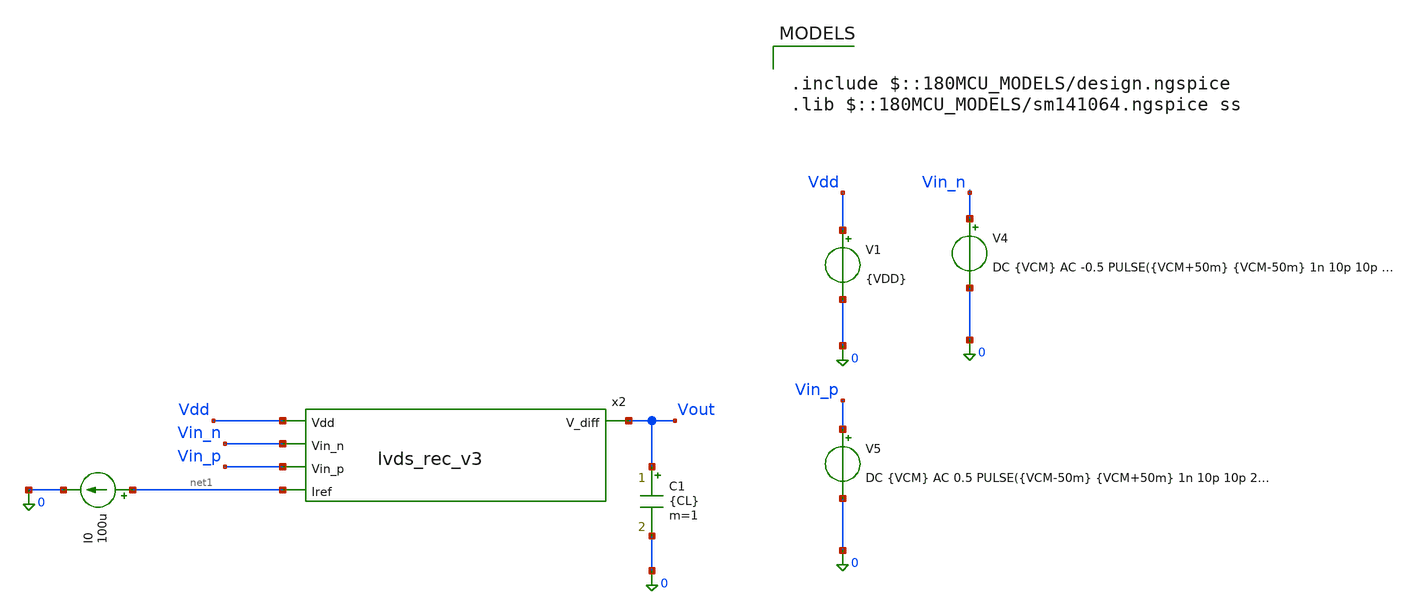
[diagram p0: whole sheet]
** sch_path: blocks/adc/lvds/ota_performance_test.sch
**.subckt ota_performance_test
V1 Vdd 0 {VDD}
V4 Vin_n 0 DC {VCM} AC -0.5 PULSE({VCM+50m} {VCM-50m} 1n 10p 10p 20n 50n)
V5 Vin_p 0 DC {VCM} AC 0.5 PULSE({VCM-50m} {VCM+50m} 1n 10p 10p 20n 50n)
C1 Vout 0 {CL} m=1
I0 net1 0 100u
x2 Vdd Vin_n Vout Vin_p net1 lvds_rec_v3
**** begin user architecture code


.param VDD=3.3
.param VSS=0
.param VCM=1.2
.param VB1=0.0
.param VB2=1.65
.param CL=100f
.options temp=125

.control
save all
set filetype=ascii
set wr_singlescale
shell rm /foss/designs/trans_testing/ota_testing/ota_ac.txt
shell rm /foss/designs/trans_testing/ota_testing/ota_tran.txt

op


* AC gain
ac dec 1000 1 500G
let vin_diff_ac = v(Vin_p)-v(Vin_n)
let gain = v(Vout)/vin_diff_ac
wrdata /foss/designs/trans_testing/ota_testing/ota_ac.txt frequency db(gain) real(gain) imag(gain)
plot v(Vout)

* Transient slew rate
tran 1p 100n
let vin_diff = v(Vin_p)-v(Vin_n)
let slew = deriv(v(Vout))
plot v(Vout)

wrdata /foss/designs/trans_testing/ota_testing/ota_tran.txt time v(Vin_p) v(Vin_n) vin_diff v(Vout)
+ slew

.endc



.include $::180MCU_MODELS/design.ngspice
.lib $::180MCU_MODELS/sm141064.ngspice ss

**** end user architecture code
**.ends

* expanding   symbol:  lvds_rec_v3.sym # of pins=5
** sym_path: blocks/adc/lvds/lvds_rec_v3.sym
** sch_path: blocks/adc/lvds/lvds_rec_v3.sch
.subckt lvds_rec_v3 Vdd Vin_n V_diff Vin_p Iref
*.ipin Vin_p
*.ipin Vin_n
*.opin V_diff
*.ipin Iref
*.ipin Vdd
x1 Vdd net1 Vin_n Vin_p Iref op_amp
x2 Vdd V_diff net1 buffer
.ends


* expanding   symbol:  op_amp.sym # of pins=5
** sym_path: blocks/adc/lvds/op_amp.sym
** sch_path: blocks/adc/lvds/op_amp.sch
.subckt op_amp Vdd Vout Vin_n Vin_p Iref
*.ipin Vdd
*.ipin Vin_p
*.ipin Vin_n
*.opin Vout
*.ipin Iref
XM1 net2 net3 Vdd Vdd pfet_03v3 L=0.28u W=10.5u nf=1 ad='int((nf+1)/2) * W/nf * 0.18u' as='int((nf+2)/2) * W/nf * 0.18u'
+ pd='2*int((nf+1)/2) * (W/nf + 0.18u)' ps='2*int((nf+2)/2) * (W/nf + 0.18u)' nrd='0.18u / W' nrs='0.18u / W'
+ sa=0 sb=0 sd=0 m=1
XM2 net1 net4 Vdd Vdd pfet_03v3 L=0.28u W=10.5u nf=1 ad='int((nf+1)/2) * W/nf * 0.18u' as='int((nf+2)/2) * W/nf * 0.18u'
+ pd='2*int((nf+1)/2) * (W/nf + 0.18u)' ps='2*int((nf+2)/2) * (W/nf + 0.18u)' nrd='0.18u / W' nrs='0.18u / W'
+ sa=0 sb=0 sd=0 m=1
XM3 net3 Vb2 net2 Vdd pfet_03v3 L=0.28u W=10.5u nf=1 ad='int((nf+1)/2) * W/nf * 0.18u' as='int((nf+2)/2) * W/nf * 0.18u'
+ pd='2*int((nf+1)/2) * (W/nf + 0.18u)' ps='2*int((nf+2)/2) * (W/nf + 0.18u)' nrd='0.18u / W' nrs='0.18u / W'
+ sa=0 sb=0 sd=0 m=1
XM4 net4 Vb2 net1 Vdd pfet_03v3 L=0.28u W=10.5u nf=1 ad='int((nf+1)/2) * W/nf * 0.18u' as='int((nf+2)/2) * W/nf * 0.18u'
+ pd='2*int((nf+1)/2) * (W/nf + 0.18u)' ps='2*int((nf+2)/2) * (W/nf + 0.18u)' nrd='0.18u / W' nrs='0.18u / W'
+ sa=0 sb=0 sd=0 m=1
XM5 net4 Vin_p net5 0 nfet_03v3 L=0.28u W=52.5u nf=15 ad='int((nf+1)/2) * W/nf * 0.18u' as='int((nf+2)/2) * W/nf * 0.18u'
+ pd='2*int((nf+1)/2) * (W/nf + 0.18u)' ps='2*int((nf+2)/2) * (W/nf + 0.18u)' nrd='0.18u / W' nrs='0.18u / W'
+ sa=0 sb=0 sd=0 m=1
XM6 net3 Vin_n net5 0 nfet_03v3 L=0.28u W=52.5u nf=15 ad='int((nf+1)/2) * W/nf * 0.18u' as='int((nf+2)/2) * W/nf * 0.18u'
+ pd='2*int((nf+1)/2) * (W/nf + 0.18u)' ps='2*int((nf+2)/2) * (W/nf + 0.18u)' nrd='0.18u / W' nrs='0.18u / W'
+ sa=0 sb=0 sd=0 m=1
XM7 net6 net4 Vdd Vdd pfet_03v3 L=0.28u W=10.5u nf=1 ad='int((nf+1)/2) * W/nf * 0.18u' as='int((nf+2)/2) * W/nf * 0.18u'
+ pd='2*int((nf+1)/2) * (W/nf + 0.18u)' ps='2*int((nf+2)/2) * (W/nf + 0.18u)' nrd='0.18u / W' nrs='0.18u / W'
+ sa=0 sb=0 sd=0 m=1
XM9 net7 net3 Vdd Vdd pfet_03v3 L=0.28u W=10.5u nf=1 ad='int((nf+1)/2) * W/nf * 0.18u' as='int((nf+2)/2) * W/nf * 0.18u'
+ pd='2*int((nf+1)/2) * (W/nf + 0.18u)' ps='2*int((nf+2)/2) * (W/nf + 0.18u)' nrd='0.18u / W' nrs='0.18u / W'
+ sa=0 sb=0 sd=0 m=1
XM11 net8 Vb2 net10 0 nfet_03v3 L=0.28u W=5.25u nf=1 ad='int((nf+1)/2) * W/nf * 0.18u' as='int((nf+2)/2) * W/nf * 0.18u'
+ pd='2*int((nf+1)/2) * (W/nf + 0.18u)' ps='2*int((nf+2)/2) * (W/nf + 0.18u)' nrd='0.18u / W' nrs='0.18u / W'
+ sa=0 sb=0 sd=0 m=1
XM12 Vout Vb2 net9 0 nfet_03v3 L=0.28u W=5.25u nf=1 ad='int((nf+1)/2) * W/nf * 0.18u' as='int((nf+2)/2) * W/nf * 0.18u'
+ pd='2*int((nf+1)/2) * (W/nf + 0.18u)' ps='2*int((nf+2)/2) * (W/nf + 0.18u)' nrd='0.18u / W' nrs='0.18u / W'
+ sa=0 sb=0 sd=0 m=1
XM13 net10 net8 0 0 nfet_03v3 L=0.28u W=5.25u nf=1 ad='int((nf+1)/2) * W/nf * 0.18u' as='int((nf+2)/2) * W/nf * 0.18u'
+ pd='2*int((nf+1)/2) * (W/nf + 0.18u)' ps='2*int((nf+2)/2) * (W/nf + 0.18u)' nrd='0.18u / W' nrs='0.18u / W'
+ sa=0 sb=0 sd=0 m=1
XM14 net9 net8 0 0 nfet_03v3 L=0.28u W=5.25u nf=1 ad='int((nf+1)/2) * W/nf * 0.18u' as='int((nf+2)/2) * W/nf * 0.18u'
+ pd='2*int((nf+1)/2) * (W/nf + 0.18u)' ps='2*int((nf+2)/2) * (W/nf + 0.18u)' nrd='0.18u / W' nrs='0.18u / W'
+ sa=0 sb=0 sd=0 m=1
XM8 net8 0 net6 Vdd pfet_03v3 L=0.28u W=10.5u nf=1 ad='int((nf+1)/2) * W/nf * 0.18u' as='int((nf+2)/2) * W/nf * 0.18u'
+ pd='2*int((nf+1)/2) * (W/nf + 0.18u)' ps='2*int((nf+2)/2) * (W/nf + 0.18u)' nrd='0.18u / W' nrs='0.18u / W'
+ sa=0 sb=0 sd=0 m=1
XM10 Vout 0 net7 Vdd pfet_03v3 L=0.28u W=10.5u nf=1 ad='int((nf+1)/2) * W/nf * 0.18u' as='int((nf+2)/2) * W/nf * 0.18u'
+ pd='2*int((nf+1)/2) * (W/nf + 0.18u)' ps='2*int((nf+2)/2) * (W/nf + 0.18u)' nrd='0.18u / W' nrs='0.18u / W'
+ sa=0 sb=0 sd=0 m=1
XM15 net5 net11 0 0 nfet_03v3 L=1u W=80u nf=20 ad='int((nf+1)/2) * W/nf * 0.18u' as='int((nf+2)/2) * W/nf * 0.18u'
+ pd='2*int((nf+1)/2) * (W/nf + 0.18u)' ps='2*int((nf+2)/2) * (W/nf + 0.18u)' nrd='0.18u / W' nrs='0.18u / W'
+ sa=0 sb=0 sd=0 m=1
XM16 Iref Iref Vdd Vdd pfet_03v3 L=1u W=20u nf=1 ad='int((nf+1)/2) * W/nf * 0.18u' as='int((nf+2)/2) * W/nf * 0.18u'
+ pd='2*int((nf+1)/2) * (W/nf + 0.18u)' ps='2*int((nf+2)/2) * (W/nf + 0.18u)' nrd='0.18u / W' nrs='0.18u / W'
+ sa=0 sb=0 sd=0 m=1
XM17 net11 Iref Vdd Vdd pfet_03v3 L=1u W=80u nf=1 ad='int((nf+1)/2) * W/nf * 0.18u' as='int((nf+2)/2) * W/nf * 0.18u'
+ pd='2*int((nf+1)/2) * (W/nf + 0.18u)' ps='2*int((nf+2)/2) * (W/nf + 0.18u)' nrd='0.18u / W' nrs='0.18u / W'
+ sa=0 sb=0 sd=0 m=1
XM18 Vb2 Iref Vdd Vdd pfet_03v3 L=1u W=20u nf=1 ad='int((nf+1)/2) * W/nf * 0.18u' as='int((nf+2)/2) * W/nf * 0.18u'
+ pd='2*int((nf+1)/2) * (W/nf + 0.18u)' ps='2*int((nf+2)/2) * (W/nf + 0.18u)' nrd='0.18u / W' nrs='0.18u / W'
+ sa=0 sb=0 sd=0 m=1
XM19 Vb2 Vb2 net12 0 nfet_03v3 L=0.28u W=30u nf=1 ad='int((nf+1)/2) * W/nf * 0.18u' as='int((nf+2)/2) * W/nf * 0.18u'
+ pd='2*int((nf+1)/2) * (W/nf + 0.18u)' ps='2*int((nf+2)/2) * (W/nf + 0.18u)' nrd='0.18u / W' nrs='0.18u / W'
+ sa=0 sb=0 sd=0 m=1
XM20 net12 net12 0 0 nfet_03v3 L=0.28u W=30u nf=1 ad='int((nf+1)/2) * W/nf * 0.18u' as='int((nf+2)/2) * W/nf * 0.18u'
+ pd='2*int((nf+1)/2) * (W/nf + 0.18u)' ps='2*int((nf+2)/2) * (W/nf + 0.18u)' nrd='0.18u / W' nrs='0.18u / W'
+ sa=0 sb=0 sd=0 m=1
XM21 net11 net11 0 0 nfet_03v3 L=1u W=80u nf=1 ad='int((nf+1)/2) * W/nf * 0.18u' as='int((nf+2)/2) * W/nf * 0.18u'
+ pd='2*int((nf+1)/2) * (W/nf + 0.18u)' ps='2*int((nf+2)/2) * (W/nf + 0.18u)' nrd='0.18u / W' nrs='0.18u / W'
+ sa=0 sb=0 sd=0 m=1
.ends


* expanding   symbol:  buffer.sym # of pins=3
** sym_path: blocks/adc/lvds/buffer.sym
** sch_path: blocks/adc/lvds/buffer.sch
.subckt buffer Vdd Vout_buff Vin
*.ipin Vdd
*.ipin Vin
*.opin Vout_buff
XM1 net1 Vin Vdd Vdd pfet_03v3 L=0.28u W=0.66u nf=1 ad='int((nf+1)/2) * W/nf * 0.18u' as='int((nf+2)/2) * W/nf * 0.18u'
+ pd='2*int((nf+1)/2) * (W/nf + 0.18u)' ps='2*int((nf+2)/2) * (W/nf + 0.18u)' nrd='0.18u / W' nrs='0.18u / W'
+ sa=0 sb=0 sd=0 m=1
XM2 net1 Vin 0 0 nfet_03v3 L=0.28u W=0.22u nf=1 ad='int((nf+1)/2) * W/nf * 0.18u' as='int((nf+2)/2) * W/nf * 0.18u'
+ pd='2*int((nf+1)/2) * (W/nf + 0.18u)' ps='2*int((nf+2)/2) * (W/nf + 0.18u)' nrd='0.18u / W' nrs='0.18u / W'
+ sa=0 sb=0 sd=0 m=1
XM3 net2 net1 Vdd Vdd pfet_03v3 L=0.28u W=2.64u nf=1 ad='int((nf+1)/2) * W/nf * 0.18u' as='int((nf+2)/2) * W/nf * 0.18u'
+ pd='2*int((nf+1)/2) * (W/nf + 0.18u)' ps='2*int((nf+2)/2) * (W/nf + 0.18u)' nrd='0.18u / W' nrs='0.18u / W'
+ sa=0 sb=0 sd=0 m=1
XM4 net2 net1 0 0 nfet_03v3 L=0.28u W=0.88u nf=1 ad='int((nf+1)/2) * W/nf * 0.18u' as='int((nf+2)/2) * W/nf * 0.18u'
+ pd='2*int((nf+1)/2) * (W/nf + 0.18u)' ps='2*int((nf+2)/2) * (W/nf + 0.18u)' nrd='0.18u / W' nrs='0.18u / W'
+ sa=0 sb=0 sd=0 m=1
XM5 net3 net2 Vdd Vdd pfet_03v3 L=0.28u W=10.56u nf=1 ad='int((nf+1)/2) * W/nf * 0.18u' as='int((nf+2)/2) * W/nf * 0.18u'
+ pd='2*int((nf+1)/2) * (W/nf + 0.18u)' ps='2*int((nf+2)/2) * (W/nf + 0.18u)' nrd='0.18u / W' nrs='0.18u / W'
+ sa=0 sb=0 sd=0 m=1
XM6 net3 net2 0 0 nfet_03v3 L=0.28u W=3.52u nf=1 ad='int((nf+1)/2) * W/nf * 0.18u' as='int((nf+2)/2) * W/nf * 0.18u'
+ pd='2*int((nf+1)/2) * (W/nf + 0.18u)' ps='2*int((nf+2)/2) * (W/nf + 0.18u)' nrd='0.18u / W' nrs='0.18u / W'
+ sa=0 sb=0 sd=0 m=1
XM7 Vout_buff net3 Vdd Vdd pfet_03v3 L=0.28u W=45u nf=1 ad='int((nf+1)/2) * W/nf * 0.18u' as='int((nf+2)/2) * W/nf * 0.18u'
+ pd='2*int((nf+1)/2) * (W/nf + 0.18u)' ps='2*int((nf+2)/2) * (W/nf + 0.18u)' nrd='0.18u / W' nrs='0.18u / W'
+ sa=0 sb=0 sd=0 m=1
XM8 Vout_buff net3 0 0 nfet_03v3 L=0.28u W=14u nf=1 ad='int((nf+1)/2) * W/nf * 0.18u' as='int((nf+2)/2) * W/nf * 0.18u'
+ pd='2*int((nf+1)/2) * (W/nf + 0.18u)' ps='2*int((nf+2)/2) * (W/nf + 0.18u)' nrd='0.18u / W' nrs='0.18u / W'
+ sa=0 sb=0 sd=0 m=1
.ends

.end
